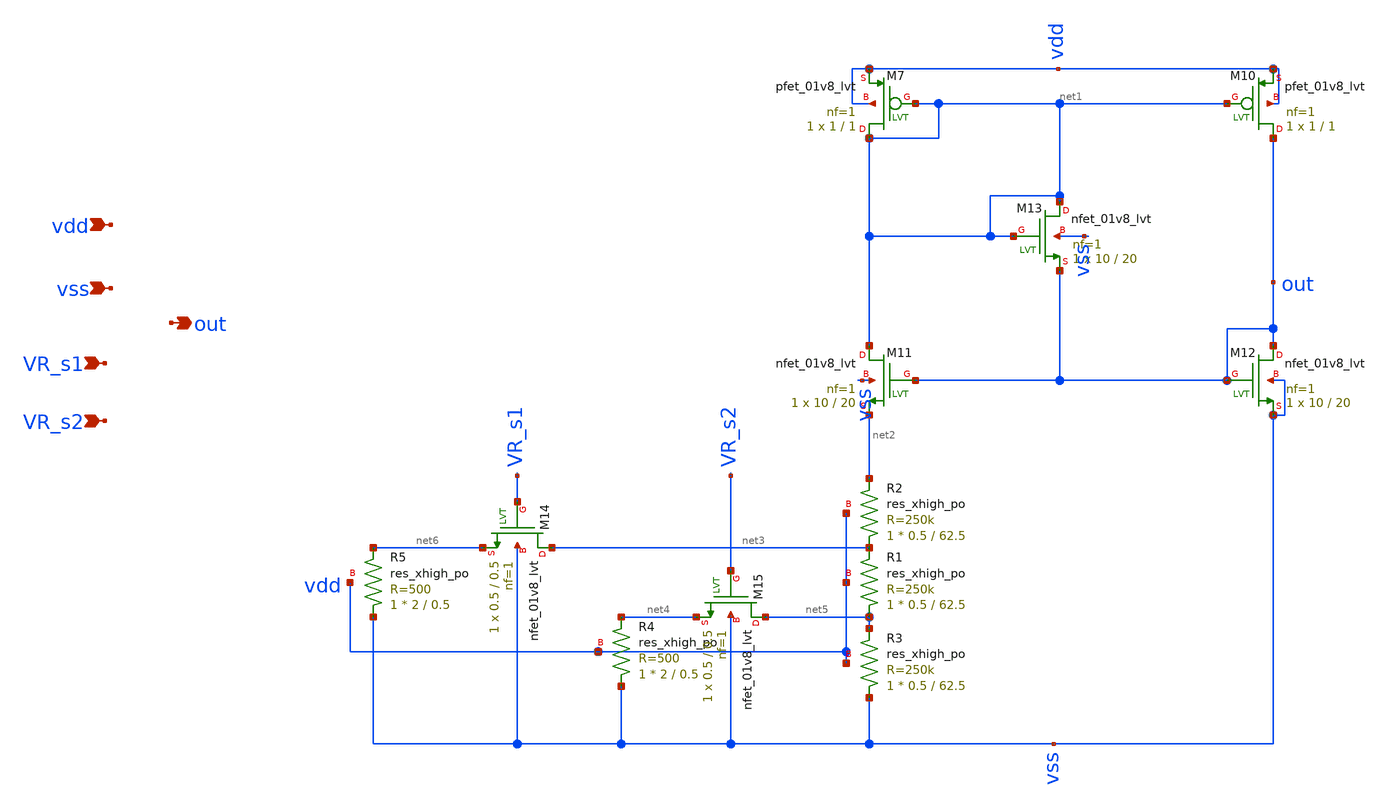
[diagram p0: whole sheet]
** sch_path: Bias.sch
**.subckt Bias vdd vss out VR_s1 VR_s2
*.ipin vdd
*.ipin vss
*.opin out
*.ipin VR_s1
*.ipin VR_s2
XM7 net1 net1 vdd vdd sky130_fd_pr__pfet_01v8_lvt L=1 W=1 nf=1 ad='int((nf+1)/2) * W/nf * 0.29' as='int((nf+2)/2) * W/nf * 0.29'
+ pd='2*int((nf+1)/2) * (W/nf + 0.29)' ps='2*int((nf+2)/2) * (W/nf + 0.29)' nrd='0.29 / W' nrs='0.29 / W'
+ sa=0 sb=0 sd=0 mult=1 m=1
XM10 out net1 vdd vdd sky130_fd_pr__pfet_01v8_lvt L=1 W=1 nf=1 ad='int((nf+1)/2) * W/nf * 0.29' as='int((nf+2)/2) * W/nf * 0.29'
+ pd='2*int((nf+1)/2) * (W/nf + 0.29)' ps='2*int((nf+2)/2) * (W/nf + 0.29)' nrd='0.29 / W' nrs='0.29 / W'
+ sa=0 sb=0 sd=0 mult=1 m=1
XM11 net1 out net2 vss sky130_fd_pr__nfet_01v8_lvt L=20 W=10 nf=1 ad='int((nf+1)/2) * W/nf * 0.29' as='int((nf+2)/2) * W/nf * 0.29'
+ pd='2*int((nf+1)/2) * (W/nf + 0.29)' ps='2*int((nf+2)/2) * (W/nf + 0.29)' nrd='0.29 / W' nrs='0.29 / W'
+ sa=0 sb=0 sd=0 mult=1 m=1
XM12 out out vss vss sky130_fd_pr__nfet_01v8_lvt L=20 W=10 nf=1 ad='int((nf+1)/2) * W/nf * 0.29' as='int((nf+2)/2) * W/nf * 0.29'
+ pd='2*int((nf+1)/2) * (W/nf + 0.29)' ps='2*int((nf+2)/2) * (W/nf + 0.29)' nrd='0.29 / W' nrs='0.29 / W'
+ sa=0 sb=0 sd=0 mult=1 m=1
XM13 net1 net1 out vss sky130_fd_pr__nfet_01v8_lvt L=20 W=10 nf=1 ad='int((nf+1)/2) * W/nf * 0.29' as='int((nf+2)/2) * W/nf * 0.29'
+ pd='2*int((nf+1)/2) * (W/nf + 0.29)' ps='2*int((nf+2)/2) * (W/nf + 0.29)' nrd='0.29 / W' nrs='0.29 / W'
+ sa=0 sb=0 sd=0 mult=1 m=1
XR1 net5 net3 vdd sky130_fd_pr__res_xhigh_po W=0.5 L=62.5 mult=1 m=1
XR2 net3 net2 vdd sky130_fd_pr__res_xhigh_po W=0.5 L=62.5 mult=1 m=1
XR3 vss net5 vdd sky130_fd_pr__res_xhigh_po W=0.5 L=62.5 mult=1 m=1
XR4 vss net4 vdd sky130_fd_pr__res_xhigh_po W=2 L=0.5 mult=1 m=1
XR5 vss net6 vdd sky130_fd_pr__res_xhigh_po W=2 L=0.5 mult=1 m=1
XM14 net3 VR_s1 net6 vss sky130_fd_pr__nfet_01v8_lvt L=0.5 W=0.5 nf=1 ad='int((nf+1)/2) * W/nf * 0.29'
+ as='int((nf+2)/2) * W/nf * 0.29' pd='2*int((nf+1)/2) * (W/nf + 0.29)' ps='2*int((nf+2)/2) * (W/nf + 0.29)'
+ nrd='0.29 / W' nrs='0.29 / W' sa=0 sb=0 sd=0 mult=1 m=1
XM15 net5 VR_s2 net4 vss sky130_fd_pr__nfet_01v8_lvt L=0.5 W=0.5 nf=1 ad='int((nf+1)/2) * W/nf * 0.29'
+ as='int((nf+2)/2) * W/nf * 0.29' pd='2*int((nf+1)/2) * (W/nf + 0.29)' ps='2*int((nf+2)/2) * (W/nf + 0.29)'
+ nrd='0.29 / W' nrs='0.29 / W' sa=0 sb=0 sd=0 mult=1 m=1
**.ends
.end
